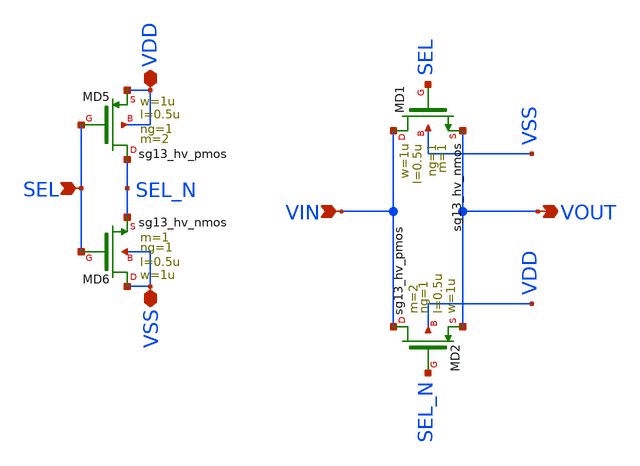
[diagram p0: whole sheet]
** sch_path: ChipUSM_AnalogTrack24/LSLH/TGVCO_vto1p1.sch
**.subckt TGVCO_vto1p1 VDD SEL VOUT VSS VIN
*.iopin VDD
*.ipin SEL
*.opin VOUT
*.iopin VSS
*.ipin VIN
XMD5 SEL_N SEL VDD VDD sg13_hv_pmos w=1u l=0.5u ng=1 m=2 mm_ok=1
XMD6 VSS SEL SEL_N VSS sg13_hv_nmos w=1u l=0.5u ng=1 m=1 mm_ok=1
XMD1 VIN SEL VOUT VSS sg13_hv_nmos w=1u l=0.5u ng=1 m=1 mm_ok=1
XMD2 VIN SEL_N VOUT VDD sg13_hv_pmos w=1u l=0.5u ng=1 m=2 mm_ok=1
**.ends
.end
